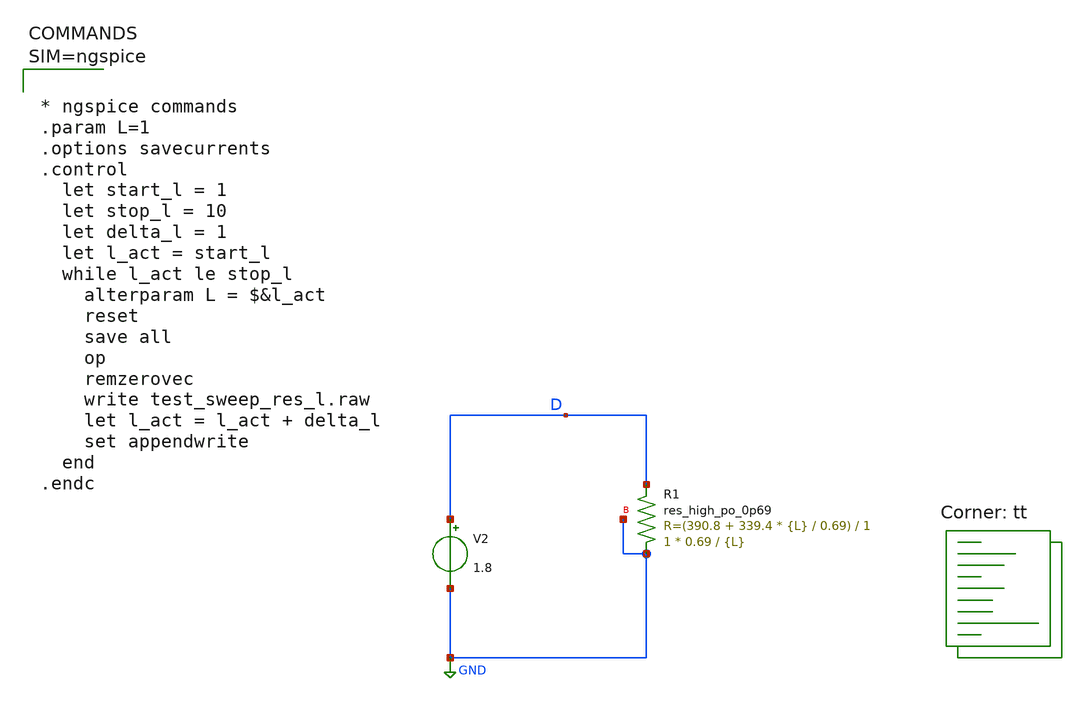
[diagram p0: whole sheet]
** sch_path: sky130A/xschem_libs/sky130_tests/test_sweep_res_l/schematic/test_sweep_res_l.sch
* Copyright 2021 Stefan Frederik Schippers
* Licensed under the Apache License, Version 2.0 (the "License");
* you may not use this file except in compliance with the License.
* You may obtain a copy of the License at
* https://www.apache.org/licenses/LICENSE-2.0
* Unless required by applicable law or agreed to in writing, software
* distributed under the License is distributed on an "AS IS" BASIS,
* WITHOUT WARRANTIES OR CONDITIONS OF ANY KIND, either express or implied.
* See the License for the specific language governing permissions and
* limitations under the License.
**.subckt test_sweep_res_l
V2 D GND 1.8
XR1 GND D GND sky130_fd_pr__res_high_po_0p69 L={L} mult=1 m=1
**** begin user architecture code
.lib $::SKYWATER_MODELS/sky130.lib.spice tt



* ngspice commands
.param L=1
.options savecurrents
.control
  let start_l = 1
  let stop_l = 10
  let delta_l = 1
  let l_act = start_l
  while l_act le stop_l
    alterparam L = $&l_act
    reset
    save all
    op
    remzerovec
    write test_sweep_res_l.raw
    let l_act = l_act + delta_l
    set appendwrite
  end
.endc



**** end user architecture code
**.ends
.GLOBAL GND
.end
